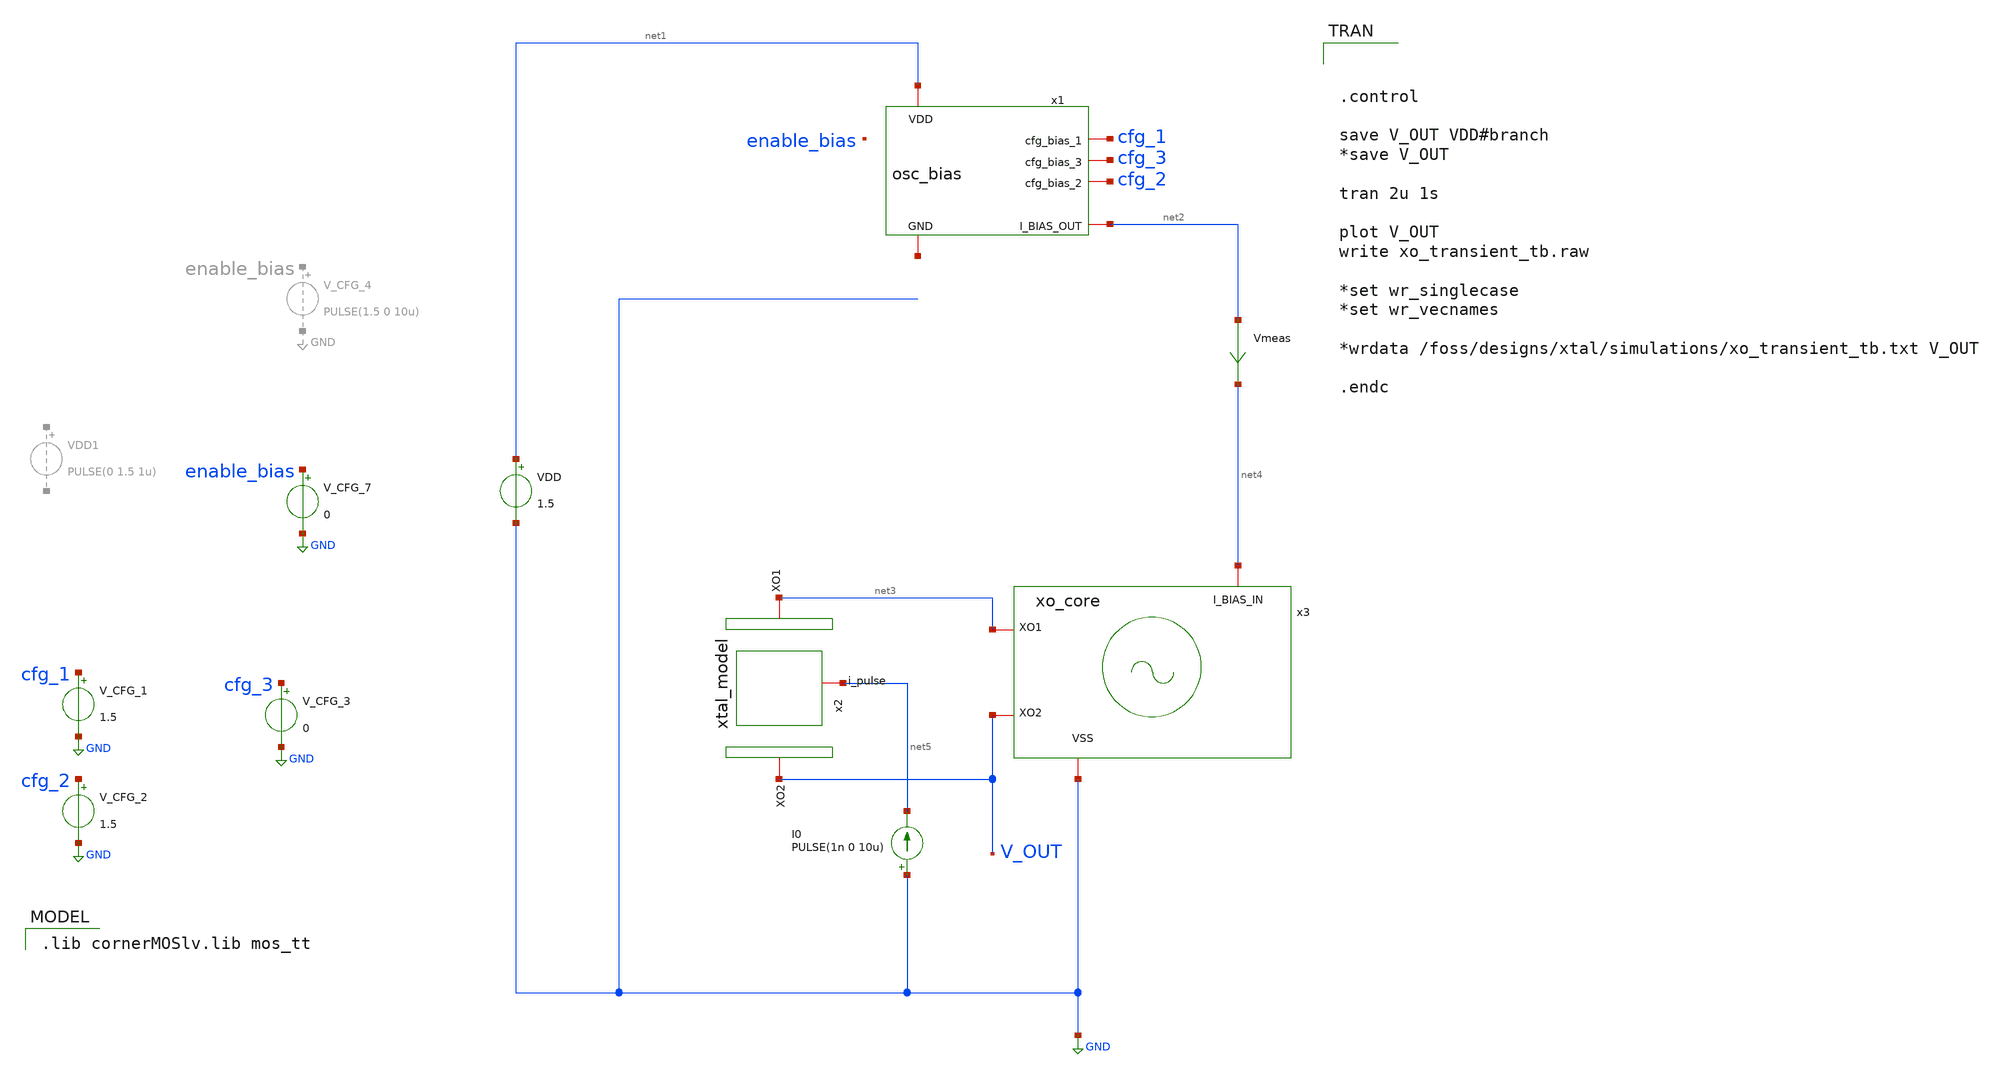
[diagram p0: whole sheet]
** sch_path: xo_transient_tb.sch
**.subckt xo_transient_tb
VDD net1 GND 1.5
x1 net1 cfg_1 cfg_3 cfg_2 net6 net2 osc_bias
x2 net3 V_OUT net5 xtal_model
x3 net4 V_OUT net3 GND xo_core
V_CFG_1 cfg_1 GND 1.5
V_CFG_2 cfg_2 GND 1.5
V_CFG_3 cfg_3 GND 0
Vmeas net2 net4 0
.save i(vmeas)
V_CFG_7 enable_bias GND 0
I0 GND net5 PULSE(1n 0 10u)
**** begin user architecture code



.control

save V_OUT VDD#branch
*save V_OUT

tran 2u 1s

plot V_OUT
write xo_transient_tb.raw

*set wr_singlecase
*set wr_vecnames

*wrdata /foss/designs/xtal/simulations/xo_transient_tb.txt V_OUT

.endc


 .lib cornerMOSlv.lib mos_tt

**** end user architecture code
**.ends

* expanding   symbol:  osc_bias.sym # of pins=6
** sym_path: osc_bias.sym
** sch_path: osc_bias.sch
.subckt osc_bias VDD cfg_bias_1 cfg_bias_3 cfg_bias_2 GND I_BIAS_OUT
*.iopin VDD
*.iopin GND
*.iopin I_BIAS_OUT
*.iopin cfg_bias_1
*.iopin cfg_bias_2
*.iopin cfg_bias_3
XM1 vp_bias vp_bias VDD VDD sg13_lv_pmos w=1u l=10u ng=1 m=1 mm_ok=1
XM3 vp_bias vp_bias net2 net1 sg13_lv_nmos w=0.25u l=10u ng=1 m=1 mm_ok=1
XM4 net2 net2 net3 net1 sg13_lv_nmos w=0.25u l=10u ng=1 m=1 mm_ok=1
XM5 net3 net3 net1 net1 sg13_lv_nmos w=0.25u l=10u ng=1 m=1 mm_ok=1
XM2 net7 vp_bias VDD VDD sg13_lv_pmos w=0.5u l=10u ng=1 m=1 mm_ok=1
XM6 I_BIAS_OUT cfg_bias_1 net7 VDD sg13_lv_pmos w=0.5u l=5u ng=1 m=1 mm_ok=1
XM7 net4 vp_bias VDD VDD sg13_lv_pmos w=0.5u l=10u ng=1 m=1 mm_ok=1
XM8 net5 vp_bias VDD VDD sg13_lv_pmos w=0.5u l=10u ng=1 m=1 mm_ok=1
XM9 I_BIAS_OUT cfg_bias_2 net4 VDD sg13_lv_pmos w=0.5u l=10u ng=1 m=1 mm_ok=1
XM10 I_BIAS_OUT cfg_bias_3 net5 VDD sg13_lv_pmos w=0.5u l=10u ng=1 m=1 mm_ok=1
XM11 net1 net1 net6 net1 sg13_lv_nmos w=0.25u l=10u ng=1 m=1 mm_ok=1
Vmeas net6 GND 0
.save i(vmeas)
.ends


* expanding   symbol:  xtal_model.sym # of pins=3
** sym_path: xtal_model.sym
** sch_path: xtal_model.sch
.subckt xtal_model XO1 XO2 i_pulse
*.iopin XO2
*.iopin XO1
*.iopin i_pulse
Rm XO1 net1 57028.5 m=1
Cm net1 i_pulse 6.408f m=1
Cp XO1 XO2 1.398p m=1
Lm i_pulse XO2 3685.8 m=1
.ends


* expanding   symbol:  xo_core.sym # of pins=4
** sym_path: xo_core.sym
** sch_path: xo_core.sch
.subckt xo_core I_BIAS_IN XO2 XO1 VSS
*.iopin VSS
*.ipin I_BIAS_IN
*.iopin XO1
*.iopin XO2
XM2 net1 XO2 XO2 XO2 sg13_lv_pmos w=0.5u l=2u ng=1 m=1 mm_ok=1
XM3 net1 XO1 XO1 XO1 sg13_lv_pmos w=0.5u l=2u ng=1 m=1 mm_ok=1
XM1 XO2 XO1 VSS VSS sg13_lv_nmos w=2.0u l=0.5u ng=1 m=1 mm_ok=1
C2 XO2 VSS 8p m=1
C1 XO1 VSS 8p m=1
Vmeas I_BIAS_IN XO2 0
.save i(vmeas)
.ends

.GLOBAL GND
.end
